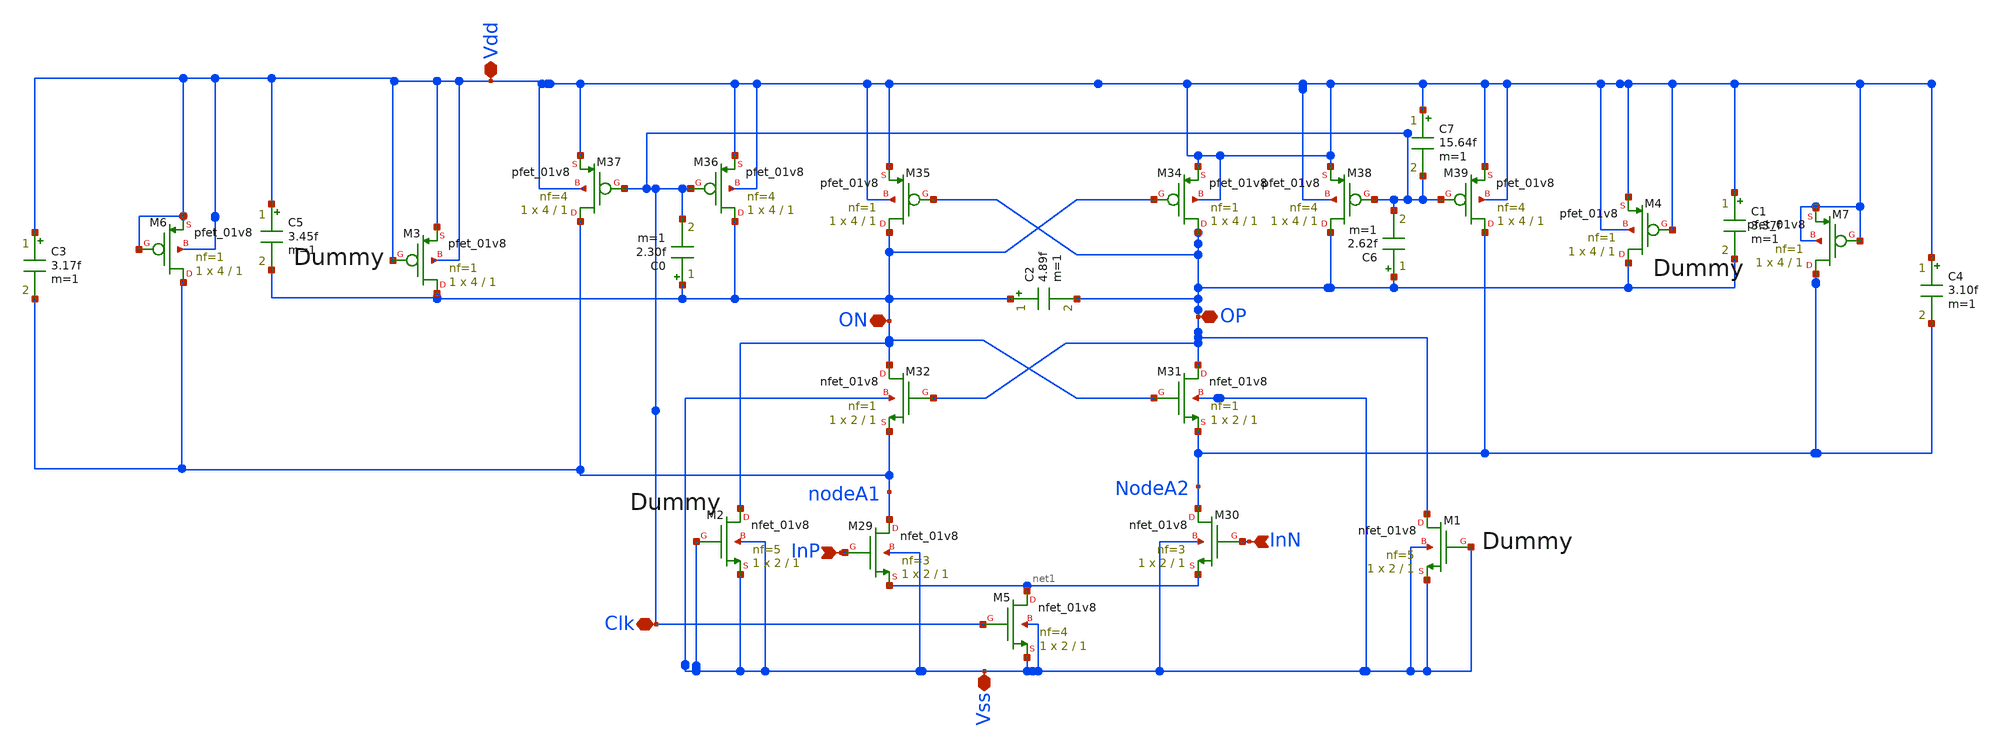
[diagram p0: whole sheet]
** sch_path: xschem/quantizer.sch
**.subckt quantizer Vss Vdd Clk InP InN ON OP
*.iopin Vss
*.iopin Vdd
*.iopin Clk
*.ipin InP
*.ipin InN
*.iopin ON
*.iopin OP
XM29 nodeA1 InP net1 Vss sky130_fd_pr__nfet_01v8 L=1 W=2 nf=3 ad='int((nf+1)/2) * W/nf * 0.29' as='int((nf+2)/2) * W/nf * 0.29'
+ pd='2*int((nf+1)/2) * (W/nf + 0.29)' ps='2*int((nf+2)/2) * (W/nf + 0.29)' nrd='0.29 / W' nrs='0.29 / W'
+ sa=0 sb=0 sd=0 mult=1 m=1
XM30 NodeA2 InN net1 Vss sky130_fd_pr__nfet_01v8 L=1 W=2 nf=3 ad='int((nf+1)/2) * W/nf * 0.29' as='int((nf+2)/2) * W/nf * 0.29'
+ pd='2*int((nf+1)/2) * (W/nf + 0.29)' ps='2*int((nf+2)/2) * (W/nf + 0.29)' nrd='0.29 / W' nrs='0.29 / W'
+ sa=0 sb=0 sd=0 mult=1 m=1
XM31 OP ON NodeA2 Vss sky130_fd_pr__nfet_01v8 L=1 W=2 nf=1 ad='int((nf+1)/2) * W/nf * 0.29' as='int((nf+2)/2) * W/nf * 0.29'
+ pd='2*int((nf+1)/2) * (W/nf + 0.29)' ps='2*int((nf+2)/2) * (W/nf + 0.29)' nrd='0.29 / W' nrs='0.29 / W'
+ sa=0 sb=0 sd=0 mult=1 m=1
XM32 ON OP nodeA1 Vss sky130_fd_pr__nfet_01v8 L=1 W=2 nf=1 ad='int((nf+1)/2) * W/nf * 0.29' as='int((nf+2)/2) * W/nf * 0.29'
+ pd='2*int((nf+1)/2) * (W/nf + 0.29)' ps='2*int((nf+2)/2) * (W/nf + 0.29)' nrd='0.29 / W' nrs='0.29 / W'
+ sa=0 sb=0 sd=0 mult=1 m=1
XM34 OP ON Vdd Vdd sky130_fd_pr__pfet_01v8 L=1 W=4 nf=1 ad='int((nf+1)/2) * W/nf * 0.29' as='int((nf+2)/2) * W/nf * 0.29'
+ pd='2*int((nf+1)/2) * (W/nf + 0.29)' ps='2*int((nf+2)/2) * (W/nf + 0.29)' nrd='0.29 / W' nrs='0.29 / W'
+ sa=0 sb=0 sd=0 mult=1 m=1
XM35 ON OP Vdd Vdd sky130_fd_pr__pfet_01v8 L=1 W=4 nf=1 ad='int((nf+1)/2) * W/nf * 0.29' as='int((nf+2)/2) * W/nf * 0.29'
+ pd='2*int((nf+1)/2) * (W/nf + 0.29)' ps='2*int((nf+2)/2) * (W/nf + 0.29)' nrd='0.29 / W' nrs='0.29 / W'
+ sa=0 sb=0 sd=0 mult=1 m=1
XM36 ON Clk Vdd Vdd sky130_fd_pr__pfet_01v8 L=1 W=4 nf=4 ad='int((nf+1)/2) * W/nf * 0.29' as='int((nf+2)/2) * W/nf * 0.29'
+ pd='2*int((nf+1)/2) * (W/nf + 0.29)' ps='2*int((nf+2)/2) * (W/nf + 0.29)' nrd='0.29 / W' nrs='0.29 / W'
+ sa=0 sb=0 sd=0 mult=1 m=1
XM37 nodeA1 Clk Vdd Vdd sky130_fd_pr__pfet_01v8 L=1 W=4 nf=4 ad='int((nf+1)/2) * W/nf * 0.29' as='int((nf+2)/2) * W/nf * 0.29'
+ pd='2*int((nf+1)/2) * (W/nf + 0.29)' ps='2*int((nf+2)/2) * (W/nf + 0.29)' nrd='0.29 / W' nrs='0.29 / W'
+ sa=0 sb=0 sd=0 mult=1 m=1
XM38 OP Clk Vdd Vdd sky130_fd_pr__pfet_01v8 L=1 W=4 nf=4 ad='int((nf+1)/2) * W/nf * 0.29' as='int((nf+2)/2) * W/nf * 0.29'
+ pd='2*int((nf+1)/2) * (W/nf + 0.29)' ps='2*int((nf+2)/2) * (W/nf + 0.29)' nrd='0.29 / W' nrs='0.29 / W'
+ sa=0 sb=0 sd=0 mult=1 m=1
XM39 NodeA2 Clk Vdd Vdd sky130_fd_pr__pfet_01v8 L=1 W=4 nf=4 ad='int((nf+1)/2) * W/nf * 0.29' as='int((nf+2)/2) * W/nf * 0.29'
+ pd='2*int((nf+1)/2) * (W/nf + 0.29)' ps='2*int((nf+2)/2) * (W/nf + 0.29)' nrd='0.29 / W' nrs='0.29 / W'
+ sa=0 sb=0 sd=0 mult=1 m=1
XM1 OP Vss Vss Vss sky130_fd_pr__nfet_01v8 L=1 W=2 nf=5 ad='int((nf+1)/2) * W/nf * 0.29' as='int((nf+2)/2) * W/nf * 0.29'
+ pd='2*int((nf+1)/2) * (W/nf + 0.29)' ps='2*int((nf+2)/2) * (W/nf + 0.29)' nrd='0.29 / W' nrs='0.29 / W'
+ sa=0 sb=0 sd=0 mult=1 m=1
XM2 ON Vss Vss Vss sky130_fd_pr__nfet_01v8 L=1 W=2 nf=5 ad='int((nf+1)/2) * W/nf * 0.29' as='int((nf+2)/2) * W/nf * 0.29'
+ pd='2*int((nf+1)/2) * (W/nf + 0.29)' ps='2*int((nf+2)/2) * (W/nf + 0.29)' nrd='0.29 / W' nrs='0.29 / W'
+ sa=0 sb=0 sd=0 mult=1 m=1
XM3 ON Vdd Vdd Vdd sky130_fd_pr__pfet_01v8 L=1 W=4 nf=1 ad='int((nf+1)/2) * W/nf * 0.29' as='int((nf+2)/2) * W/nf * 0.29'
+ pd='2*int((nf+1)/2) * (W/nf + 0.29)' ps='2*int((nf+2)/2) * (W/nf + 0.29)' nrd='0.29 / W' nrs='0.29 / W'
+ sa=0 sb=0 sd=0 mult=1 m=1
XM4 OP Vdd Vdd Vdd sky130_fd_pr__pfet_01v8 L=1 W=4 nf=1 ad='int((nf+1)/2) * W/nf * 0.29' as='int((nf+2)/2) * W/nf * 0.29'
+ pd='2*int((nf+1)/2) * (W/nf + 0.29)' ps='2*int((nf+2)/2) * (W/nf + 0.29)' nrd='0.29 / W' nrs='0.29 / W'
+ sa=0 sb=0 sd=0 mult=1 m=1
XM5 net1 Clk Vss Vss sky130_fd_pr__nfet_01v8 L=1 W=2 nf=4 ad='int((nf+1)/2) * W/nf * 0.29' as='int((nf+2)/2) * W/nf * 0.29'
+ pd='2*int((nf+1)/2) * (W/nf + 0.29)' ps='2*int((nf+2)/2) * (W/nf + 0.29)' nrd='0.29 / W' nrs='0.29 / W'
+ sa=0 sb=0 sd=0 mult=1 m=1
XM6 nodeA1 Vdd Vdd Vdd sky130_fd_pr__pfet_01v8 L=1 W=4 nf=1 ad='int((nf+1)/2) * W/nf * 0.29' as='int((nf+2)/2) * W/nf * 0.29'
+ pd='2*int((nf+1)/2) * (W/nf + 0.29)' ps='2*int((nf+2)/2) * (W/nf + 0.29)' nrd='0.29 / W' nrs='0.29 / W'
+ sa=0 sb=0 sd=0 mult=1 m=1
XM7 NodeA2 Vdd Vdd Vdd sky130_fd_pr__pfet_01v8 L=1 W=4 nf=1 ad='int((nf+1)/2) * W/nf * 0.29' as='int((nf+2)/2) * W/nf * 0.29'
+ pd='2*int((nf+1)/2) * (W/nf + 0.29)' ps='2*int((nf+2)/2) * (W/nf + 0.29)' nrd='0.29 / W' nrs='0.29 / W'
+ sa=0 sb=0 sd=0 mult=1 m=1
C4 Vdd NodeA2 3.10f m=1
C3 Vdd nodeA1 3.17f m=1
C1 Vdd OP 3.37f m=1
C5 Vdd ON 3.45f m=1
C2 ON OP 4.89f m=1
C7 Vdd Clk 15.64f m=1
C6 OP Clk 2.62f m=1
C0 ON Clk 2.30f m=1
**.ends
.end
